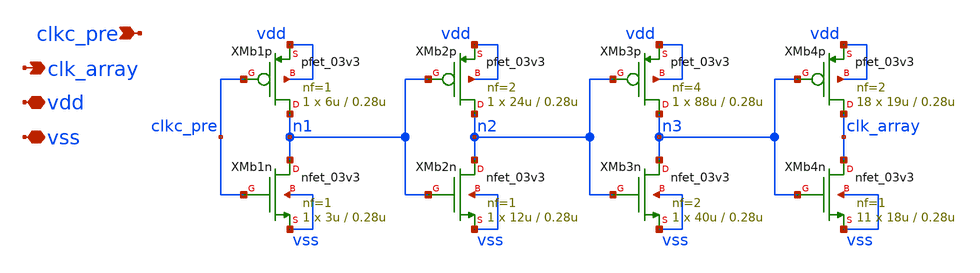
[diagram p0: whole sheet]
** sch_path: blocks/adc/comp-array/compact/clkbuf.sch
**.subckt clkbuf clk_array vdd vss clkc_pre
*.opin clk_array
*.iopin vdd
*.iopin vss
*.ipin clkc_pre
XMb1n n1 clkc_pre vss vss nfet_03v3 L=0.28u W=3u nf=1 ad='int((nf+1)/2) * W/nf * 0.18u' as='int((nf+2)/2) * W/nf * 0.18u'
+ pd='2*int((nf+1)/2) * (W/nf + 0.18u)' ps='2*int((nf+2)/2) * (W/nf + 0.18u)' nrd='0.18u / W' nrs='0.18u / W'
+ sa=0 sb=0 sd=0 m=1
XMb1p n1 clkc_pre vdd vdd pfet_03v3 L=0.28u W=6u nf=1 ad='int((nf+1)/2) * W/nf * 0.18u' as='int((nf+2)/2) * W/nf * 0.18u'
+ pd='2*int((nf+1)/2) * (W/nf + 0.18u)' ps='2*int((nf+2)/2) * (W/nf + 0.18u)' nrd='0.18u / W' nrs='0.18u / W'
+ sa=0 sb=0 sd=0 m=1
XMb2n n2 n1 vss vss nfet_03v3 L=0.28u W=12u nf=1 ad='int((nf+1)/2) * W/nf * 0.18u' as='int((nf+2)/2) * W/nf * 0.18u'
+ pd='2*int((nf+1)/2) * (W/nf + 0.18u)' ps='2*int((nf+2)/2) * (W/nf + 0.18u)' nrd='0.18u / W' nrs='0.18u / W'
+ sa=0 sb=0 sd=0 m=1
XMb2p n2 n1 vdd vdd pfet_03v3 L=0.28u W=24u nf=2 ad='int((nf+1)/2) * W/nf * 0.18u' as='int((nf+2)/2) * W/nf * 0.18u'
+ pd='2*int((nf+1)/2) * (W/nf + 0.18u)' ps='2*int((nf+2)/2) * (W/nf + 0.18u)' nrd='0.18u / W' nrs='0.18u / W'
+ sa=0 sb=0 sd=0 m=1
XMb3n n3 n2 vss vss nfet_03v3 L=0.28u W=40u nf=2 ad='int((nf+1)/2) * W/nf * 0.18u' as='int((nf+2)/2) * W/nf * 0.18u'
+ pd='2*int((nf+1)/2) * (W/nf + 0.18u)' ps='2*int((nf+2)/2) * (W/nf + 0.18u)' nrd='0.18u / W' nrs='0.18u / W'
+ sa=0 sb=0 sd=0 m=1
XMb3p n3 n2 vdd vdd pfet_03v3 L=0.28u W=88u nf=4 ad='int((nf+1)/2) * W/nf * 0.18u' as='int((nf+2)/2) * W/nf * 0.18u'
+ pd='2*int((nf+1)/2) * (W/nf + 0.18u)' ps='2*int((nf+2)/2) * (W/nf + 0.18u)' nrd='0.18u / W' nrs='0.18u / W'
+ sa=0 sb=0 sd=0 m=1
XMb4n clk_array n3 vss vss nfet_03v3 L=0.28u W=18u nf=1 ad='int((nf+1)/2) * W/nf * 0.18u' as='int((nf+2)/2) * W/nf * 0.18u'
+ pd='2*int((nf+1)/2) * (W/nf + 0.18u)' ps='2*int((nf+2)/2) * (W/nf + 0.18u)' nrd='0.18u / W' nrs='0.18u / W'
+ sa=0 sb=0 sd=0 m=11
XMb4p clk_array n3 vdd vdd pfet_03v3 L=0.28u W=19u nf=2 ad='int((nf+1)/2) * W/nf * 0.18u' as='int((nf+2)/2) * W/nf * 0.18u'
+ pd='2*int((nf+1)/2) * (W/nf + 0.18u)' ps='2*int((nf+2)/2) * (W/nf + 0.18u)' nrd='0.18u / W' nrs='0.18u / W'
+ sa=0 sb=0 sd=0 m=18
**.ends
.end
